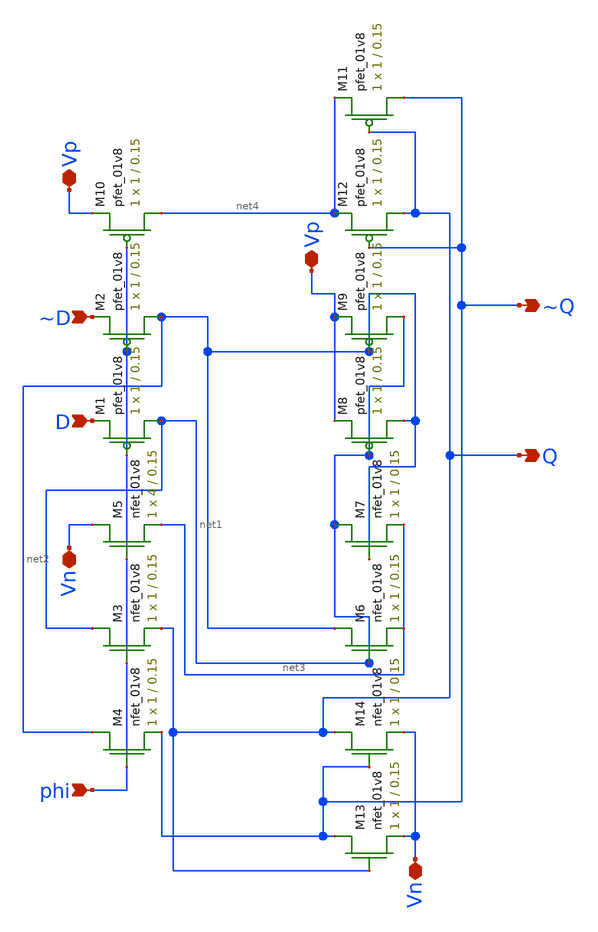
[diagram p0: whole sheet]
** sch_path: mini_proj_2/schematic/d_flip_flop_2.sch
**.subckt d_flip_flop_2 phi D ~D Vp Vp ~Q Q Vn Vn
*.ipin phi
*.ipin D
*.ipin ~D
*.iopin Vp
*.iopin Vp
*.opin ~Q
*.opin Q
*.iopin Vn
*.iopin Vn
XM4 net2 phi ~Q GND sky130_fd_pr__nfet_01v8 L=0.15 W=1 nf=1 ad='int((nf+1)/2) * W/nf * 0.29' as='int((nf+2)/2) * W/nf * 0.29'
+ pd='2*int((nf+1)/2) * (W/nf + 0.29)' ps='2*int((nf+2)/2) * (W/nf + 0.29)' nrd='0.29 / W' nrs='0.29 / W'
+ sa=0 sb=0 sd=0 mult=1 m=1
XM3 net1 phi Q GND sky130_fd_pr__nfet_01v8 L=0.15 W=1 nf=1 ad='int((nf+1)/2) * W/nf * 0.29' as='int((nf+2)/2) * W/nf * 0.29'
+ pd='2*int((nf+1)/2) * (W/nf + 0.29)' ps='2*int((nf+2)/2) * (W/nf + 0.29)' nrd='0.29 / W' nrs='0.29 / W'
+ sa=0 sb=0 sd=0 mult=1 m=1
XM1 net1 phi D VDD sky130_fd_pr__pfet_01v8 L=0.15 W=1 nf=1 ad='int((nf+1)/2) * W/nf * 0.29' as='int((nf+2)/2) * W/nf * 0.29'
+ pd='2*int((nf+1)/2) * (W/nf + 0.29)' ps='2*int((nf+2)/2) * (W/nf + 0.29)' nrd='0.29 / W' nrs='0.29 / W'
+ sa=0 sb=0 sd=0 mult=1 m=1
XM2 net2 phi ~D VDD sky130_fd_pr__pfet_01v8 L=0.15 W=1 nf=1 ad='int((nf+1)/2) * W/nf * 0.29' as='int((nf+2)/2) * W/nf * 0.29'
+ pd='2*int((nf+1)/2) * (W/nf + 0.29)' ps='2*int((nf+2)/2) * (W/nf + 0.29)' nrd='0.29 / W' nrs='0.29 / W'
+ sa=0 sb=0 sd=0 mult=1 m=1
XM10 net4 phi Vp VDD sky130_fd_pr__pfet_01v8 L=0.15 W=1 nf=1 ad='int((nf+1)/2) * W/nf * 0.29' as='int((nf+2)/2) * W/nf * 0.29'
+ pd='2*int((nf+1)/2) * (W/nf + 0.29)' ps='2*int((nf+2)/2) * (W/nf + 0.29)' nrd='0.29 / W' nrs='0.29 / W'
+ sa=0 sb=0 sd=0 mult=1 m=1
XM13 ~Q Q Vn GND sky130_fd_pr__nfet_01v8 L=0.15 W=1 nf=1 ad='int((nf+1)/2) * W/nf * 0.29' as='int((nf+2)/2) * W/nf * 0.29'
+ pd='2*int((nf+1)/2) * (W/nf + 0.29)' ps='2*int((nf+2)/2) * (W/nf + 0.29)' nrd='0.29 / W' nrs='0.29 / W'
+ sa=0 sb=0 sd=0 mult=1 m=1
XM14 Q ~Q Vn GND sky130_fd_pr__nfet_01v8 L=0.15 W=1 nf=1 ad='int((nf+1)/2) * W/nf * 0.29' as='int((nf+2)/2) * W/nf * 0.29'
+ pd='2*int((nf+1)/2) * (W/nf + 0.29)' ps='2*int((nf+2)/2) * (W/nf + 0.29)' nrd='0.29 / W' nrs='0.29 / W'
+ sa=0 sb=0 sd=0 mult=1 m=1
XM6 net2 net1 net3 GND sky130_fd_pr__nfet_01v8 L=0.15 W=1 nf=1 ad='int((nf+1)/2) * W/nf * 0.29' as='int((nf+2)/2) * W/nf * 0.29'
+ pd='2*int((nf+1)/2) * (W/nf + 0.29)' ps='2*int((nf+2)/2) * (W/nf + 0.29)' nrd='0.29 / W' nrs='0.29 / W'
+ sa=0 sb=0 sd=0 mult=1 m=1
XM7 net1 net2 net3 GND sky130_fd_pr__nfet_01v8 L=0.15 W=1 nf=1 ad='int((nf+1)/2) * W/nf * 0.29' as='int((nf+2)/2) * W/nf * 0.29'
+ pd='2*int((nf+1)/2) * (W/nf + 0.29)' ps='2*int((nf+2)/2) * (W/nf + 0.29)' nrd='0.29 / W' nrs='0.29 / W'
+ sa=0 sb=0 sd=0 mult=1 m=1
XM5 Vn phi net3 GND sky130_fd_pr__nfet_01v8 L=0.15 W=4 nf=1 ad='int((nf+1)/2) * W/nf * 0.29' as='int((nf+2)/2) * W/nf * 0.29'
+ pd='2*int((nf+1)/2) * (W/nf + 0.29)' ps='2*int((nf+2)/2) * (W/nf + 0.29)' nrd='0.29 / W' nrs='0.29 / W'
+ sa=0 sb=0 sd=0 mult=1 m=1
XM8 net2 net1 Vp VDD sky130_fd_pr__pfet_01v8 L=0.15 W=1 nf=1 ad='int((nf+1)/2) * W/nf * 0.29' as='int((nf+2)/2) * W/nf * 0.29'
+ pd='2*int((nf+1)/2) * (W/nf + 0.29)' ps='2*int((nf+2)/2) * (W/nf + 0.29)' nrd='0.29 / W' nrs='0.29 / W'
+ sa=0 sb=0 sd=0 mult=1 m=1
XM9 net1 net2 Vp VDD sky130_fd_pr__pfet_01v8 L=0.15 W=1 nf=1 ad='int((nf+1)/2) * W/nf * 0.29' as='int((nf+2)/2) * W/nf * 0.29'
+ pd='2*int((nf+1)/2) * (W/nf + 0.29)' ps='2*int((nf+2)/2) * (W/nf + 0.29)' nrd='0.29 / W' nrs='0.29 / W'
+ sa=0 sb=0 sd=0 mult=1 m=1
XM12 Q ~Q net4 VDD sky130_fd_pr__pfet_01v8 L=0.15 W=1 nf=1 ad='int((nf+1)/2) * W/nf * 0.29' as='int((nf+2)/2) * W/nf * 0.29'
+ pd='2*int((nf+1)/2) * (W/nf + 0.29)' ps='2*int((nf+2)/2) * (W/nf + 0.29)' nrd='0.29 / W' nrs='0.29 / W'
+ sa=0 sb=0 sd=0 mult=1 m=1
XM11 ~Q Q net4 VDD sky130_fd_pr__pfet_01v8 L=0.15 W=1 nf=1 ad='int((nf+1)/2) * W/nf * 0.29' as='int((nf+2)/2) * W/nf * 0.29'
+ pd='2*int((nf+1)/2) * (W/nf + 0.29)' ps='2*int((nf+2)/2) * (W/nf + 0.29)' nrd='0.29 / W' nrs='0.29 / W'
+ sa=0 sb=0 sd=0 mult=1 m=1
**.ends
.end
